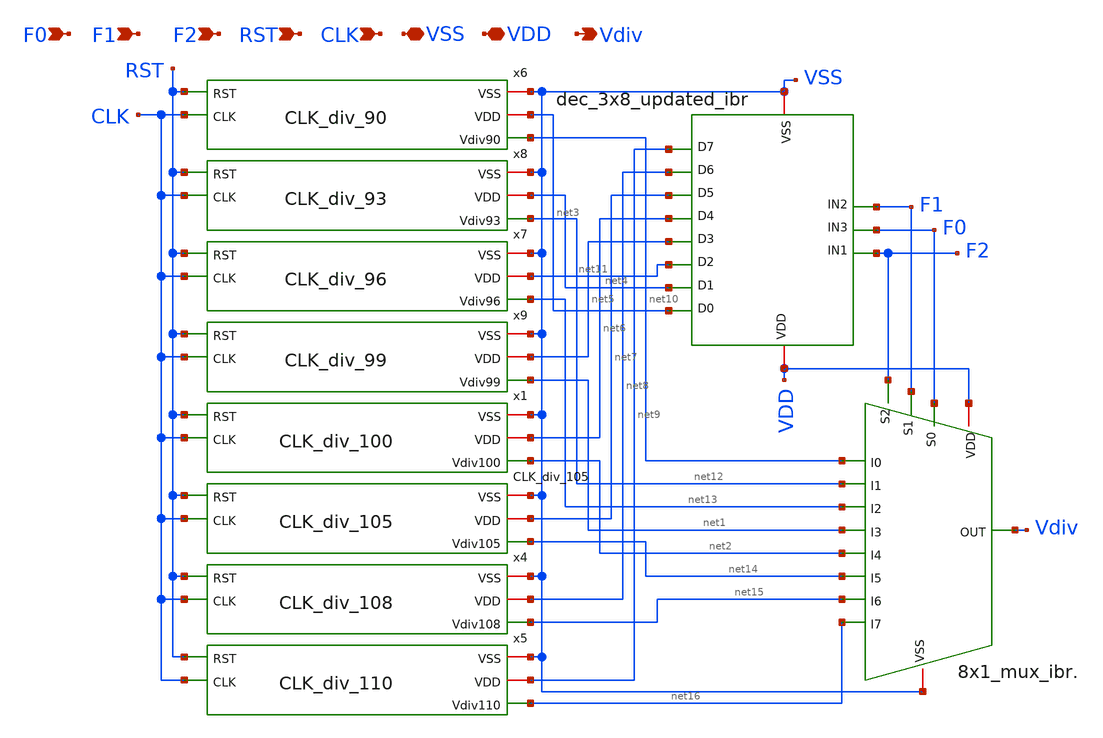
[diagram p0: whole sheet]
** sch_path: Clock_Generator_PAKISTAN_02/Schematics/Feedback_Divider.sch
**.subckt Feedback_Divider CLK VSS VDD RST Vdiv F2 F1 F0
*.ipin CLK
*.iopin VSS
*.iopin VDD
*.ipin RST
*.opin Vdiv
*.ipin F2
*.ipin F1
*.ipin F0
x1 VSS net6 RST net2 CLK CLK_div_100
x4 VSS net8 RST net15 CLK CLK_div_108
x5 VSS net9 RST net16 CLK CLK_div_110
x6 VSS net3 RST net10 CLK CLK_div_90
x7 VSS net11 RST net13 CLK CLK_div_96
x8 VSS net4 net12 RST CLK CLK_div_93
x9 VSS net5 net1 RST CLK CLK_div_99
x2 VDD VSS F1 F0 Vdiv F2 net10 net16 net1 net13 net14 net12 net2 net15 8x1_mux_ibr.
x10 F2 VSS VDD net3 net4 net11 net5 net6 net7 net8 net9 F0 F1 dec_3x8_updated_ibr
x3 VSS net7 RST net14 CLK CLK_div_105
**.ends
.end
